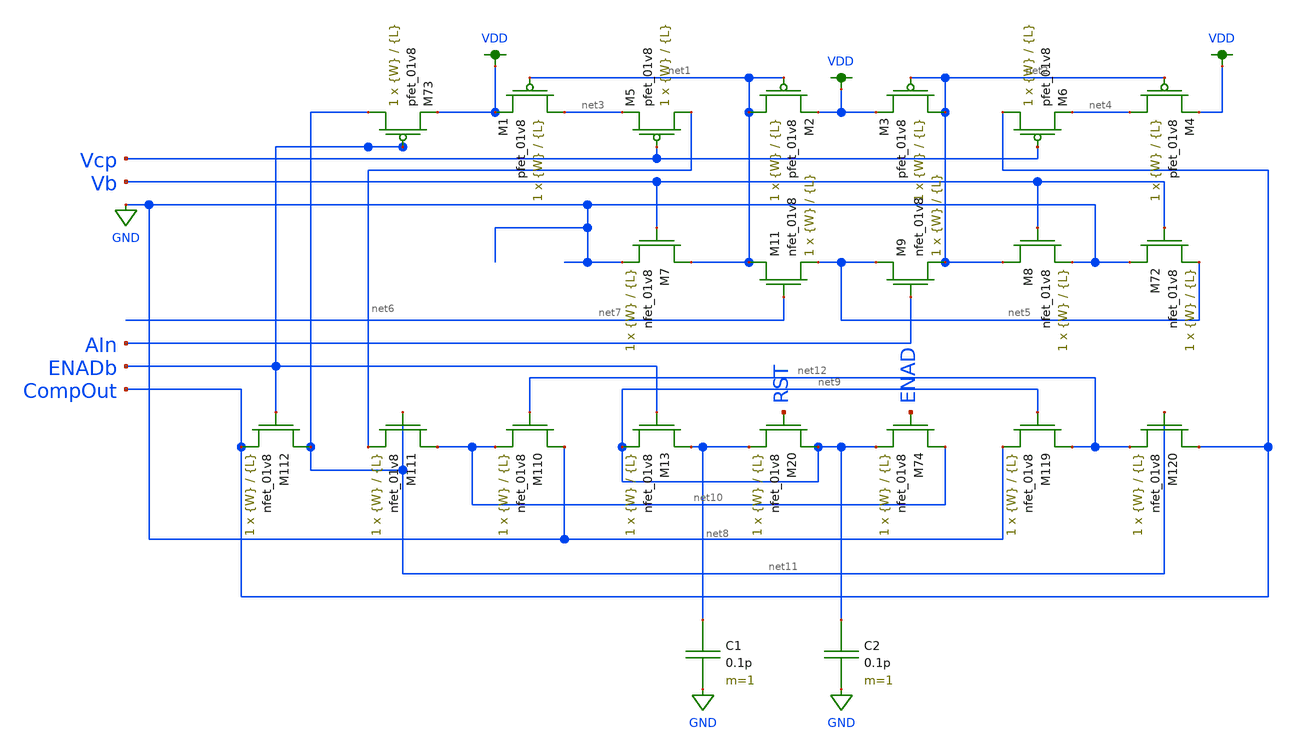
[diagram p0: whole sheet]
** sch_path: schematics/Comparator_LDS_James.sch
**.subckt Comparator_LDS_James
XM1 net3 net1 VDD VDD sky130_fd_pr__pfet_01v8 L={L} W={W} nf=1 ad='int((nf+1)/2) * W/nf * 0.29' as='int((nf+2)/2) * W/nf * 0.29'
+ pd='2*int((nf+1)/2) * (W/nf + 0.29)' ps='2*int((nf+2)/2) * (W/nf + 0.29)' nrd='0.29 / W' nrs='0.29 / W'
+ sa=0 sb=0 sd=0 mult=1 m=1
XM2 net1 net1 VDD VDD sky130_fd_pr__pfet_01v8 L={L} W={W} nf=1 ad='int((nf+1)/2) * W/nf * 0.29' as='int((nf+2)/2) * W/nf * 0.29'
+ pd='2*int((nf+1)/2) * (W/nf + 0.29)' ps='2*int((nf+2)/2) * (W/nf + 0.29)' nrd='0.29 / W' nrs='0.29 / W'
+ sa=0 sb=0 sd=0 mult=1 m=1
XM3 net2 net2 VDD VDD sky130_fd_pr__pfet_01v8 L={L} W={W} nf=1 ad='int((nf+1)/2) * W/nf * 0.29' as='int((nf+2)/2) * W/nf * 0.29'
+ pd='2*int((nf+1)/2) * (W/nf + 0.29)' ps='2*int((nf+2)/2) * (W/nf + 0.29)' nrd='0.29 / W' nrs='0.29 / W'
+ sa=0 sb=0 sd=0 mult=1 m=1
XM4 net4 net2 VDD VDD sky130_fd_pr__pfet_01v8 L={L} W={W} nf=1 ad='int((nf+1)/2) * W/nf * 0.29' as='int((nf+2)/2) * W/nf * 0.29'
+ pd='2*int((nf+1)/2) * (W/nf + 0.29)' ps='2*int((nf+2)/2) * (W/nf + 0.29)' nrd='0.29 / W' nrs='0.29 / W'
+ sa=0 sb=0 sd=0 mult=1 m=1
XM5 net6 Vcp net3 VDD sky130_fd_pr__pfet_01v8 L={L} W={W} nf=1 ad='int((nf+1)/2) * W/nf * 0.29' as='int((nf+2)/2) * W/nf * 0.29'
+ pd='2*int((nf+1)/2) * (W/nf + 0.29)' ps='2*int((nf+2)/2) * (W/nf + 0.29)' nrd='0.29 / W' nrs='0.29 / W'
+ sa=0 sb=0 sd=0 mult=1 m=1
XM6 CompOut Vcp net4 VDD sky130_fd_pr__pfet_01v8 L={L} W={W} nf=1 ad='int((nf+1)/2) * W/nf * 0.29' as='int((nf+2)/2) * W/nf * 0.29'
+ pd='2*int((nf+1)/2) * (W/nf + 0.29)' ps='2*int((nf+2)/2) * (W/nf + 0.29)' nrd='0.29 / W' nrs='0.29 / W'
+ sa=0 sb=0 sd=0 mult=1 m=1
XM7 net1 Vb GND GND sky130_fd_pr__nfet_01v8 L={L} W={W} nf=1 ad='int((nf+1)/2) * W/nf * 0.29' as='int((nf+2)/2) * W/nf * 0.29'
+ pd='2*int((nf+1)/2) * (W/nf + 0.29)' ps='2*int((nf+2)/2) * (W/nf + 0.29)' nrd='0.29 / W' nrs='0.29 / W'
+ sa=0 sb=0 sd=0 mult=1 m=1
XM8 net2 Vb GND GND sky130_fd_pr__nfet_01v8 L={L} W={W} nf=1 ad='int((nf+1)/2) * W/nf * 0.29' as='int((nf+2)/2) * W/nf * 0.29'
+ pd='2*int((nf+1)/2) * (W/nf + 0.29)' ps='2*int((nf+2)/2) * (W/nf + 0.29)' nrd='0.29 / W' nrs='0.29 / W'
+ sa=0 sb=0 sd=0 mult=1 m=1
XM9 net5 AIn net2 GND sky130_fd_pr__nfet_01v8 L={L} W={W} nf=1 ad='int((nf+1)/2) * W/nf * 0.29' as='int((nf+2)/2) * W/nf * 0.29'
+ pd='2*int((nf+1)/2) * (W/nf + 0.29)' ps='2*int((nf+2)/2) * (W/nf + 0.29)' nrd='0.29 / W' nrs='0.29 / W'
+ sa=0 sb=0 sd=0 mult=1 m=1
XM11 net1 net7 net5 GND sky130_fd_pr__nfet_01v8 L={L} W={W} nf=1 ad='int((nf+1)/2) * W/nf * 0.29' as='int((nf+2)/2) * W/nf * 0.29'
+ pd='2*int((nf+1)/2) * (W/nf + 0.29)' ps='2*int((nf+2)/2) * (W/nf + 0.29)' nrd='0.29 / W' nrs='0.29 / W'
+ sa=0 sb=0 sd=0 mult=1 m=1
XM20 net9 RST net8 GND sky130_fd_pr__nfet_01v8 L={L} W={W} nf=1 ad='int((nf+1)/2) * W/nf * 0.29' as='int((nf+2)/2) * W/nf * 0.29'
+ pd='2*int((nf+1)/2) * (W/nf + 0.29)' ps='2*int((nf+2)/2) * (W/nf + 0.29)' nrd='0.29 / W' nrs='0.29 / W'
+ sa=0 sb=0 sd=0 mult=1 m=1
C1 net8 GND 0.1p m=1
C2 net9 GND 0.1p m=1
XM72 GND Vb net5 GND sky130_fd_pr__nfet_01v8 L={L} W={W} nf=1 ad='int((nf+1)/2) * W/nf * 0.29' as='int((nf+2)/2) * W/nf * 0.29'
+ pd='2*int((nf+1)/2) * (W/nf + 0.29)' ps='2*int((nf+2)/2) * (W/nf + 0.29)' nrd='0.29 / W' nrs='0.29 / W'
+ sa=0 sb=0 sd=0 mult=1 m=1
XM73 net11 ENADb VDD VDD sky130_fd_pr__pfet_01v8 L={L} W={W} nf=1 ad='int((nf+1)/2) * W/nf * 0.29' as='int((nf+2)/2) * W/nf * 0.29'
+ pd='2*int((nf+1)/2) * (W/nf + 0.29)' ps='2*int((nf+2)/2) * (W/nf + 0.29)' nrd='0.29 / W' nrs='0.29 / W'
+ sa=0 sb=0 sd=0 mult=1 m=1
XM13 net8 ENADb net9 GND sky130_fd_pr__nfet_01v8 L={L} W={W} nf=1 ad='int((nf+1)/2) * W/nf * 0.29' as='int((nf+2)/2) * W/nf * 0.29'
+ pd='2*int((nf+1)/2) * (W/nf + 0.29)' ps='2*int((nf+2)/2) * (W/nf + 0.29)' nrd='0.29 / W' nrs='0.29 / W'
+ sa=0 sb=0 sd=0 mult=1 m=1
XM74 net10 ENAD net9 GND sky130_fd_pr__nfet_01v8 L={L} W={W} nf=1 ad='int((nf+1)/2) * W/nf * 0.29' as='int((nf+2)/2) * W/nf * 0.29'
+ pd='2*int((nf+1)/2) * (W/nf + 0.29)' ps='2*int((nf+2)/2) * (W/nf + 0.29)' nrd='0.29 / W' nrs='0.29 / W'
+ sa=0 sb=0 sd=0 mult=1 m=1
XM110 GND net12 net10 GND sky130_fd_pr__nfet_01v8 L={L} W={W} nf=1 ad='int((nf+1)/2) * W/nf * 0.29' as='int((nf+2)/2) * W/nf * 0.29'
+ pd='2*int((nf+1)/2) * (W/nf + 0.29)' ps='2*int((nf+2)/2) * (W/nf + 0.29)' nrd='0.29 / W' nrs='0.29 / W'
+ sa=0 sb=0 sd=0 mult=1 m=1
XM111 net10 net11 net6 GND sky130_fd_pr__nfet_01v8 L={L} W={W} nf=1 ad='int((nf+1)/2) * W/nf * 0.29'
+ as='int((nf+2)/2) * W/nf * 0.29' pd='2*int((nf+1)/2) * (W/nf + 0.29)' ps='2*int((nf+2)/2) * (W/nf + 0.29)'
+ nrd='0.29 / W' nrs='0.29 / W' sa=0 sb=0 sd=0 mult=1 m=1
XM112 net11 ENADb CompOut GND sky130_fd_pr__nfet_01v8 L={L} W={W} nf=1 ad='int((nf+1)/2) * W/nf * 0.29'
+ as='int((nf+2)/2) * W/nf * 0.29' pd='2*int((nf+1)/2) * (W/nf + 0.29)' ps='2*int((nf+2)/2) * (W/nf + 0.29)'
+ nrd='0.29 / W' nrs='0.29 / W' sa=0 sb=0 sd=0 mult=1 m=1
XM119 net12 net9 GND GND sky130_fd_pr__nfet_01v8 L={L} W={W} nf=1 ad='int((nf+1)/2) * W/nf * 0.29' as='int((nf+2)/2) * W/nf * 0.29'
+ pd='2*int((nf+1)/2) * (W/nf + 0.29)' ps='2*int((nf+2)/2) * (W/nf + 0.29)' nrd='0.29 / W' nrs='0.29 / W'
+ sa=0 sb=0 sd=0 mult=1 m=1
XM120 CompOut net11 net12 GND sky130_fd_pr__nfet_01v8 L={L} W={W} nf=1 ad='int((nf+1)/2) * W/nf * 0.29'
+ as='int((nf+2)/2) * W/nf * 0.29' pd='2*int((nf+1)/2) * (W/nf + 0.29)' ps='2*int((nf+2)/2) * (W/nf + 0.29)'
+ nrd='0.29 / W' nrs='0.29 / W' sa=0 sb=0 sd=0 mult=1 m=1
**.ends
.GLOBAL GND
.GLOBAL VDD
.end
